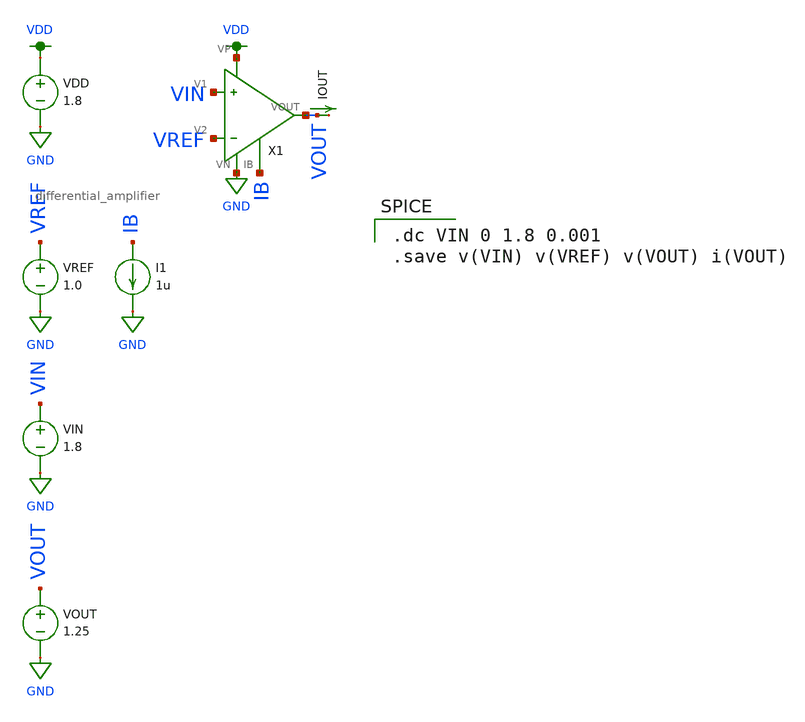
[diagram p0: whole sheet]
** sch_path: mp3/schematics/differential_amplifier_tran_b.sch
**.subckt differential_amplifier_tran_b
VDD VDD GND 1.8
I1 IB GND 1u
VREF VREF GND 1.0
VIN VIN GND 1.8
X1 VIN VREF VDD GND IB VOUT differential_amplifier
VOUT VOUT GND 1.25
IOUT VOUT net1 0
.save i(iout)
**** begin user architecture code

.option wnflag=1
.lib ~/skywater/skywater-pdk/libraries/sky130_fd_pr_ngspice/latest/models/sky130.lib.spice tt


.dc VIN 0 1.8 0.001
.save v(VIN) v(VREF) v(VOUT) i(VOUT)

**** end user architecture code
**.ends
.GLOBAL GND
.GLOBAL VDD
.end
